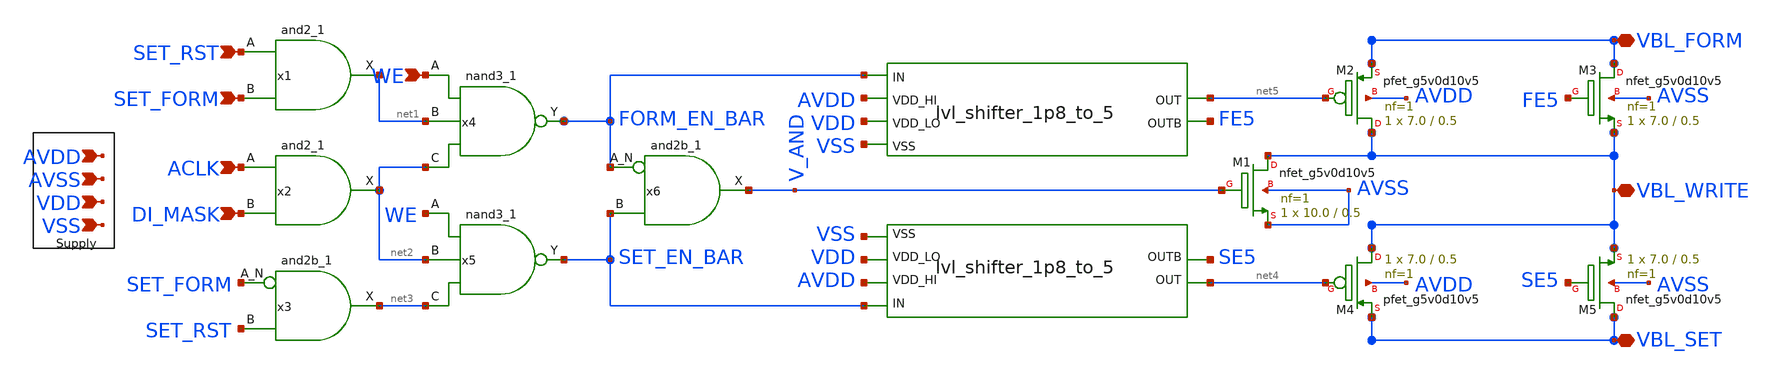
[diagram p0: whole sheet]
** sch_path: BL_SL_Writing_Interface/BL_driver.sch
**.subckt BL_driver VSS VDD WE SET_RST SET_FORM ACLK DI_MASK AVDD VBL_SET VBL_FORM VBL_WRITE AVSS
*.ipin VSS
*.ipin VDD
*.ipin WE
*.ipin SET_RST
*.ipin SET_FORM
*.ipin ACLK
*.ipin DI_MASK
*.ipin AVDD
*.iopin VBL_SET
*.iopin VBL_FORM
*.iopin VBL_WRITE
*.ipin AVSS
x1 SET_RST SET_FORM VSS VSS VDD VDD net1 sky130_fd_sc_hd__and2_1
x2 ACLK DI_MASK VSS VSS VDD VDD net2 sky130_fd_sc_hd__and2_1
x3 SET_FORM SET_RST VSS VSS VDD VDD net3 sky130_fd_sc_hd__and2b_1
x4 WE net1 net2 VSS VSSS VDD VDD FORM_EN_BAR sky130_fd_sc_hd__nand3_1
x5 WE net2 net3 VSS VSSS VDD VDD SET_EN_BAR sky130_fd_sc_hd__nand3_1
x6 FORM_EN_BAR SET_EN_BAR VSS VSS VDD VDD V_AND sky130_fd_sc_hd__and2b_1
XM5 VBL_SET SE5 VBL_WRITE AVSS sky130_fd_pr__nfet_g5v0d10v5 L=0.5 W=7.0 nf=1 ad='int((nf+1)/2) * W/nf * 0.29'
+ as='int((nf+2)/2) * W/nf * 0.29' pd='2*int((nf+1)/2) * (W/nf + 0.29)' ps='2*int((nf+2)/2) * (W/nf + 0.29)'
+ nrd='0.29 / W' nrs='0.29 / W' sa=0 sb=0 sd=0 mult=1 m=1
XM4 VBL_WRITE net4 VBL_SET AVDD sky130_fd_pr__pfet_g5v0d10v5 L=0.5 W=7.0 nf=1 ad='int((nf+1)/2) * W/nf * 0.29'
+ as='int((nf+2)/2) * W/nf * 0.29' pd='2*int((nf+1)/2) * (W/nf + 0.29)' ps='2*int((nf+2)/2) * (W/nf + 0.29)'
+ nrd='0.29 / W' nrs='0.29 / W' sa=0 sb=0 sd=0 mult=1 m=1
XM2 VBL_WRITE net5 VBL_FORM AVDD sky130_fd_pr__pfet_g5v0d10v5 L=0.5 W=7.0 nf=1 ad='int((nf+1)/2) * W/nf * 0.29'
+ as='int((nf+2)/2) * W/nf * 0.29' pd='2*int((nf+1)/2) * (W/nf + 0.29)' ps='2*int((nf+2)/2) * (W/nf + 0.29)'
+ nrd='0.29 / W' nrs='0.29 / W' sa=0 sb=0 sd=0 mult=1 m=1
XM3 VBL_FORM FE5 VBL_WRITE AVSS sky130_fd_pr__nfet_g5v0d10v5 L=0.5 W=7.0 nf=1 ad='int((nf+1)/2) * W/nf * 0.29'
+ as='int((nf+2)/2) * W/nf * 0.29' pd='2*int((nf+1)/2) * (W/nf + 0.29)' ps='2*int((nf+2)/2) * (W/nf + 0.29)'
+ nrd='0.29 / W' nrs='0.29 / W' sa=0 sb=0 sd=0 mult=1 m=1
XM1 VBL_WRITE V_AND AVSS AVSS sky130_fd_pr__nfet_g5v0d10v5 L=0.5 W=10.0 nf=1 ad='int((nf+1)/2) * W/nf * 0.29'
+ as='int((nf+2)/2) * W/nf * 0.29' pd='2*int((nf+1)/2) * (W/nf + 0.29)' ps='2*int((nf+2)/2) * (W/nf + 0.29)'
+ nrd='0.29 / W' nrs='0.29 / W' sa=0 sb=0 sd=0 mult=1 m=1
x1 AVDD FE5 net5 VDD FORM_EN_BAR VSS lvl_shifter_1p8_to_5
x1 AVDD SE5 net4 VDD SET_EN_BAR VSS lvl_shifter_1p8_to_5
**.ends

* expanding   symbol:  lvl_shifter_1p8_to_5.sym # of pins=6
** sym_path: BL_SL_Writing_Interface/lvl_shifter_1p8_to_5.sym
** sch_path: BL_SL_Writing_Interface/lvl_shifter_1p8_to_5.sch
.subckt lvl_shifter_1p8_to_5 VDD_HI OUTB OUT VDD_LO IN VSS
*.ipin VDD_HI
*.opin OUT
*.opin OUTB
*.ipin IN
*.ipin VDD_LO
*.ipin VSS
XM5 net1 IN VSS VSS sky130_fd_pr__nfet_01v8 L=0.15 W=0.42 nf=1 ad='int((nf+1)/2) * W/nf * 0.29' as='int((nf+2)/2) * W/nf * 0.29'
+ pd='2*int((nf+1)/2) * (W/nf + 0.29)' ps='2*int((nf+2)/2) * (W/nf + 0.29)' nrd='0.29 / W' nrs='0.29 / W'
+ sa=0 sb=0 sd=0 mult=1 m=1
XM7 net2 net1 VSS VSS sky130_fd_pr__nfet_01v8 L=0.15 W=0.42 nf=1 ad='int((nf+1)/2) * W/nf * 0.29' as='int((nf+2)/2) * W/nf * 0.29'
+ pd='2*int((nf+1)/2) * (W/nf + 0.29)' ps='2*int((nf+2)/2) * (W/nf + 0.29)' nrd='0.29 / W' nrs='0.29 / W'
+ sa=0 sb=0 sd=0 mult=1 m=1
XM3 net1 IN VDD_LO VDD_LO sky130_fd_pr__pfet_01v8 L=0.15 W=0.84 nf=1 ad='int((nf+1)/2) * W/nf * 0.29'
+ as='int((nf+2)/2) * W/nf * 0.29' pd='2*int((nf+1)/2) * (W/nf + 0.29)' ps='2*int((nf+2)/2) * (W/nf + 0.29)'
+ nrd='0.29 / W' nrs='0.29 / W' sa=0 sb=0 sd=0 mult=1 m=1
XM4 net2 net1 VDD_LO VDD_LO sky130_fd_pr__pfet_01v8 L=0.15 W=0.84 nf=1 ad='int((nf+1)/2) * W/nf * 0.29'
+ as='int((nf+2)/2) * W/nf * 0.29' pd='2*int((nf+1)/2) * (W/nf + 0.29)' ps='2*int((nf+2)/2) * (W/nf + 0.29)'
+ nrd='0.29 / W' nrs='0.29 / W' sa=0 sb=0 sd=0 mult=1 m=1
XM6 OUT net1 VSS VSS sky130_fd_pr__nfet_g5v0d10v5 L=0.5 W=5 nf=1 ad='int((nf+1)/2) * W/nf * 0.29' as='int((nf+2)/2) * W/nf * 0.29'
+ pd='2*int((nf+1)/2) * (W/nf + 0.29)' ps='2*int((nf+2)/2) * (W/nf + 0.29)' nrd='0.29 / W' nrs='0.29 / W'
+ sa=0 sb=0 sd=0 mult=1 m=1
XM8 OUTB net2 VSS VSS sky130_fd_pr__nfet_g5v0d10v5 L=0.5 W=5 nf=1 ad='int((nf+1)/2) * W/nf * 0.29' as='int((nf+2)/2) * W/nf * 0.29'
+ pd='2*int((nf+1)/2) * (W/nf + 0.29)' ps='2*int((nf+2)/2) * (W/nf + 0.29)' nrd='0.29 / W' nrs='0.29 / W'
+ sa=0 sb=0 sd=0 mult=1 m=1
XM1 OUT OUTB VDD_HI VDD_HI sky130_fd_pr__pfet_g5v0d10v5 L=0.5 W=1.5 nf=1 ad='int((nf+1)/2) * W/nf * 0.29'
+ as='int((nf+2)/2) * W/nf * 0.29' pd='2*int((nf+1)/2) * (W/nf + 0.29)' ps='2*int((nf+2)/2) * (W/nf + 0.29)'
+ nrd='0.29 / W' nrs='0.29 / W' sa=0 sb=0 sd=0 mult=1 m=1
XM2 OUTB OUT VDD_HI VDD_HI sky130_fd_pr__pfet_g5v0d10v5 L=0.5 W=1.5 nf=1 ad='int((nf+1)/2) * W/nf * 0.29'
+ as='int((nf+2)/2) * W/nf * 0.29' pd='2*int((nf+1)/2) * (W/nf + 0.29)' ps='2*int((nf+2)/2) * (W/nf + 0.29)'
+ nrd='0.29 / W' nrs='0.29 / W' sa=0 sb=0 sd=0 mult=1 m=1
.ends

.end
